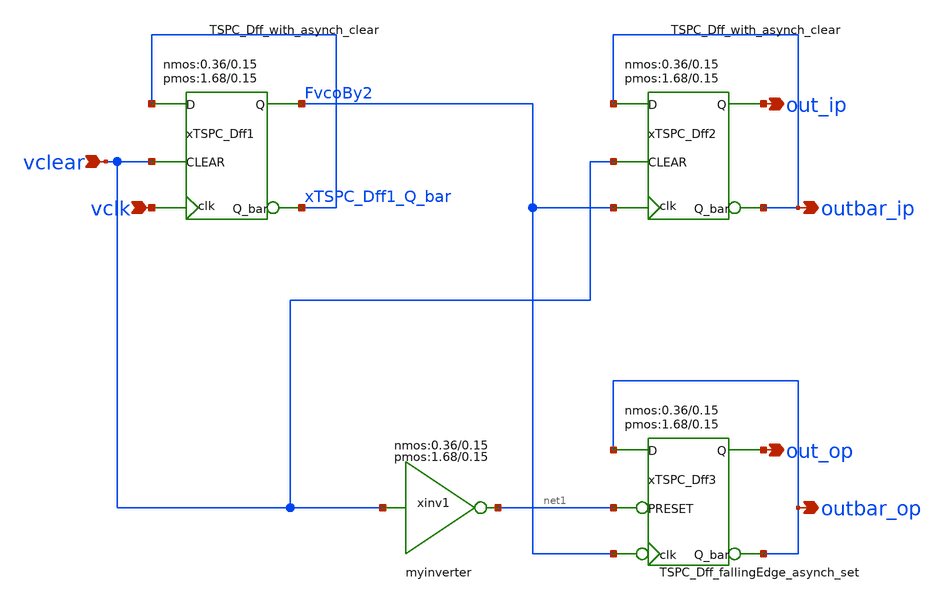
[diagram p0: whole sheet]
** sch_path: freqDivideby4.sch
**.subckt freqDivideby4 vclear vclk out_ip outbar_ip out_op outbar_op
*.ipin vclear
*.ipin vclk
*.opin out_ip
*.opin outbar_ip
*.opin out_op
*.opin outbar_op
xTSPC_Dff1 vclk xTSPC_Dff1_Q_bar xTSPC_Dff1_Q_bar FvcoBy2 vclear VDD GND TSPC_Dff_with_asynch_clear
+ wnmos=0.36 lnmos=0.15 wpmos=1.68 lpmos=0.15 m=1
xTSPC_Dff2 FvcoBy2 outbar_ip outbar_ip out_ip vclear VDD GND TSPC_Dff_with_asynch_clear wnmos=0.36
+ lnmos=0.15 wpmos=1.68 lpmos=0.15 m=1
xTSPC_Dff3 FvcoBy2 outbar_op outbar_op out_op net1 VDD GND TSPC_Dff_fallingEdge_asynch_set
+ wnmos=0.36 lnmos=0.15 wpmos=1.68 lpmos=0.15 m=1
xinv1 vclear net1 VDD VSS myinverter wnmos=0.36 lnmos=0.15 wpmos=1.68 lpmos=0.15 m=1
**.ends
.end
